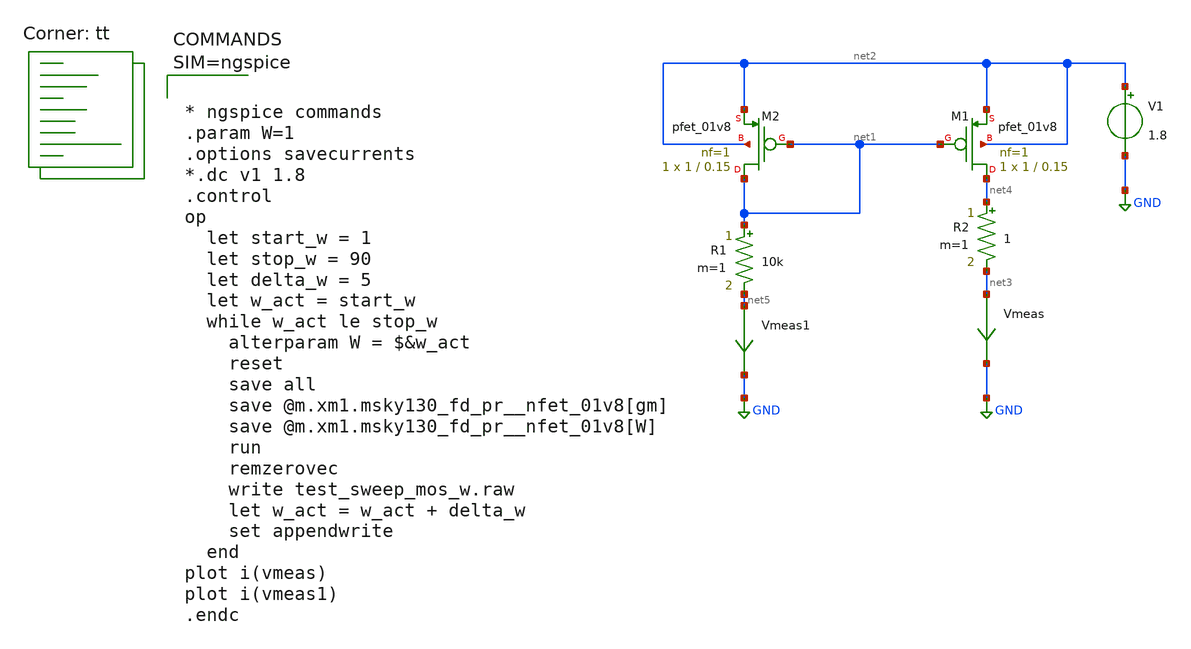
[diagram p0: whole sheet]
** sch_path: xschem/Specchio.sch
**.subckt Specchio
XM1 net4 net1 net2 net2 sky130_fd_pr__pfet_01v8 L=0.15 W=1 nf=1 ad='int((nf+1)/2) * W/nf * 0.29' as='int((nf+2)/2) * W/nf * 0.29'
+ pd='2*int((nf+1)/2) * (W/nf + 0.29)' ps='2*int((nf+2)/2) * (W/nf + 0.29)' nrd='0.29 / W' nrs='0.29 / W'
+ sa=0 sb=0 sd=0 mult=1 m=1
XM2 net1 net1 net2 net2 sky130_fd_pr__pfet_01v8 L=0.15 W=1 nf=1 ad='int((nf+1)/2) * W/nf * 0.29' as='int((nf+2)/2) * W/nf * 0.29'
+ pd='2*int((nf+1)/2) * (W/nf + 0.29)' ps='2*int((nf+2)/2) * (W/nf + 0.29)' nrd='0.29 / W' nrs='0.29 / W'
+ sa=0 sb=0 sd=0 mult=1 m=1
R1 net1 net5 10k m=1
Vmeas net3 GND 0
.save i(vmeas)
V1 net2 GND 1.8
R2 net4 net3 1 m=1
Vmeas1 net5 GND 0
.save i(vmeas1)
**** begin user architecture code
.lib $::SKYWATER_MODELS/sky130.lib.spice tt



* ngspice commands
.param W=1
.options savecurrents
*.dc v1 1.8
.control
op
  let start_w = 1
  let stop_w = 90
  let delta_w = 5
  let w_act = start_w
  while w_act le stop_w
    alterparam W = $&w_act
    reset
    save all
    save @m.xm1.msky130_fd_pr__nfet_01v8[gm]
    save @m.xm1.msky130_fd_pr__nfet_01v8[W]
    run
    remzerovec
    write test_sweep_mos_w.raw
    let w_act = w_act + delta_w
    set appendwrite
  end
plot i(vmeas)
plot i(vmeas1)
.endc



**** end user architecture code
**.ends
.GLOBAL GND
.end
